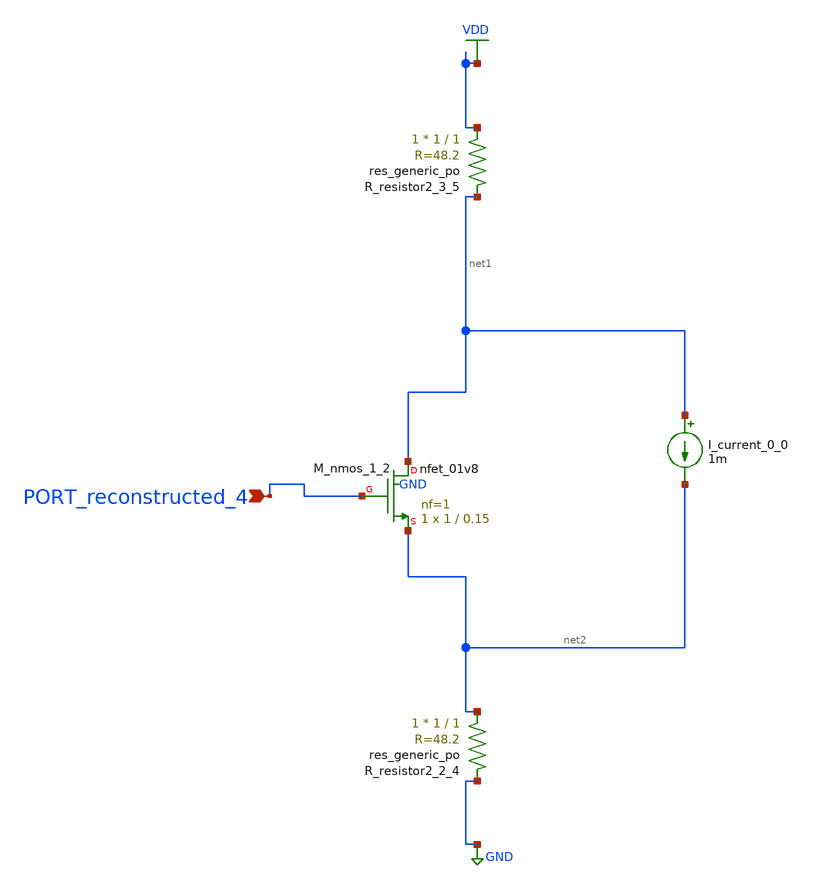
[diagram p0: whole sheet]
** sch_path: schematics/AMSNet/483.sch
**.subckt 483 PORT_reconstructed_4
*.ipin PORT_reconstructed_4
I_current_0_0 net1 net2 1m
XM_nmos_1_2 net1 PORT_reconstructed_4 net2 GND sky130_fd_pr__nfet_01v8 L=0.15 W=1 nf=1 ad='int((1 + 1)/2) * 1 / 1 * 0.29'
+ as='int((1 + 2)/2) * 1 / 1 * 0.29' pd='2*int((1 + 1)/2) * (1 / 1 + 0.29)' ps='2*int((1 + 2)/2) * (1 / 1 + 0.29)'
+ nrd='0.29 / 1 ' nrs='0.29 / 1 ' sa=0 sb=0 sd=0 mult=1 m=1
XR_resistor2_2_4 net2 GND sky130_fd_pr__res_generic_po W=1 L=1 m=1
XR_resistor2_3_5 VDD net1 sky130_fd_pr__res_generic_po W=1 L=1 m=1
**.ends
.GLOBAL GND
.GLOBAL VDD
.end
